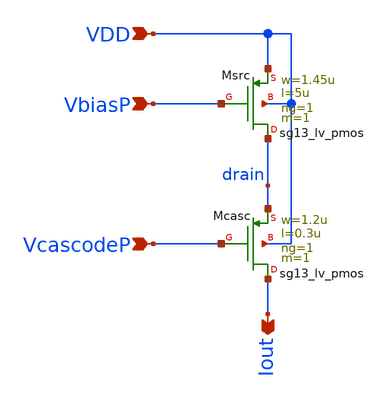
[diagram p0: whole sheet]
** sch_path: xschem/pcsource2u.sch
**.subckt pcsource2u VcascodeP VbiasP Iout VDD
*.ipin VcascodeP
*.ipin VbiasP
*.opin Iout
*.ipin VDD
XMsrc drain VbiasP VDD VDD sg13_lv_pmos w=1.45u l=5u ng=1 m=1 mm_ok=1
XMcasc Iout VcascodeP drain VDD sg13_lv_pmos w=1.2u l=0.3u ng=1 m=1 mm_ok=1
**.ends
.end
